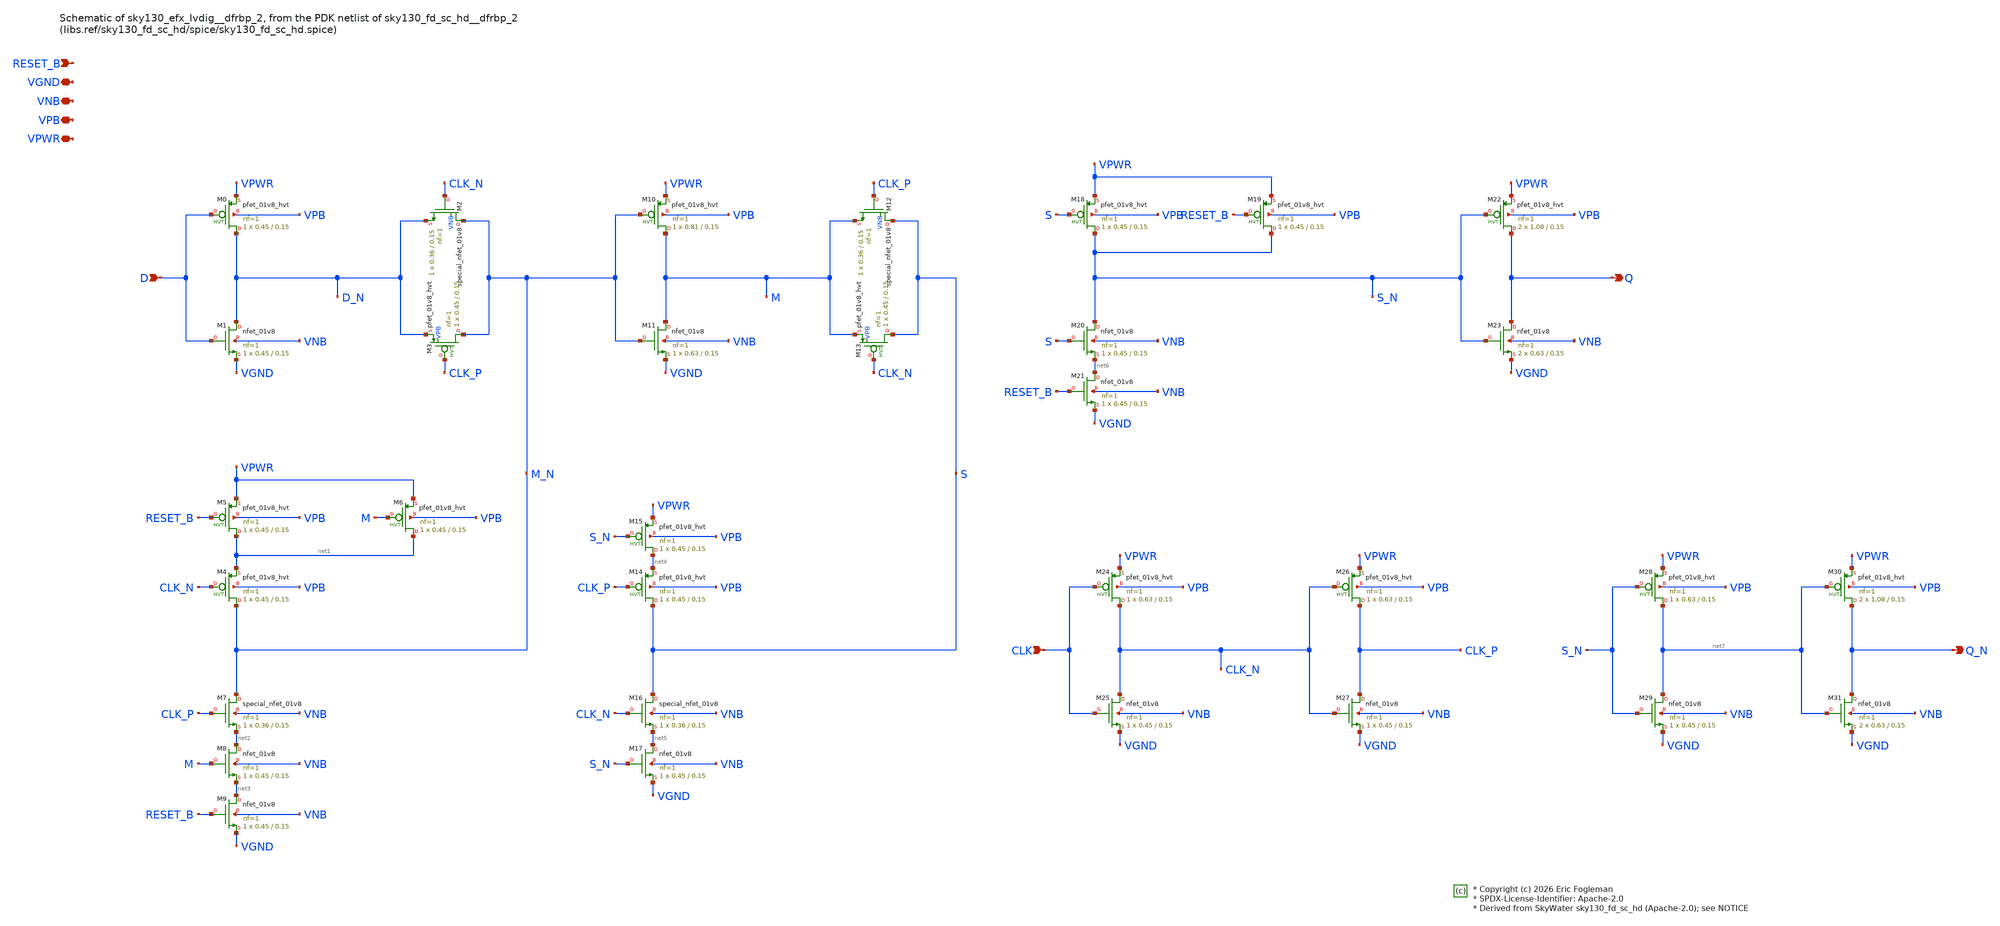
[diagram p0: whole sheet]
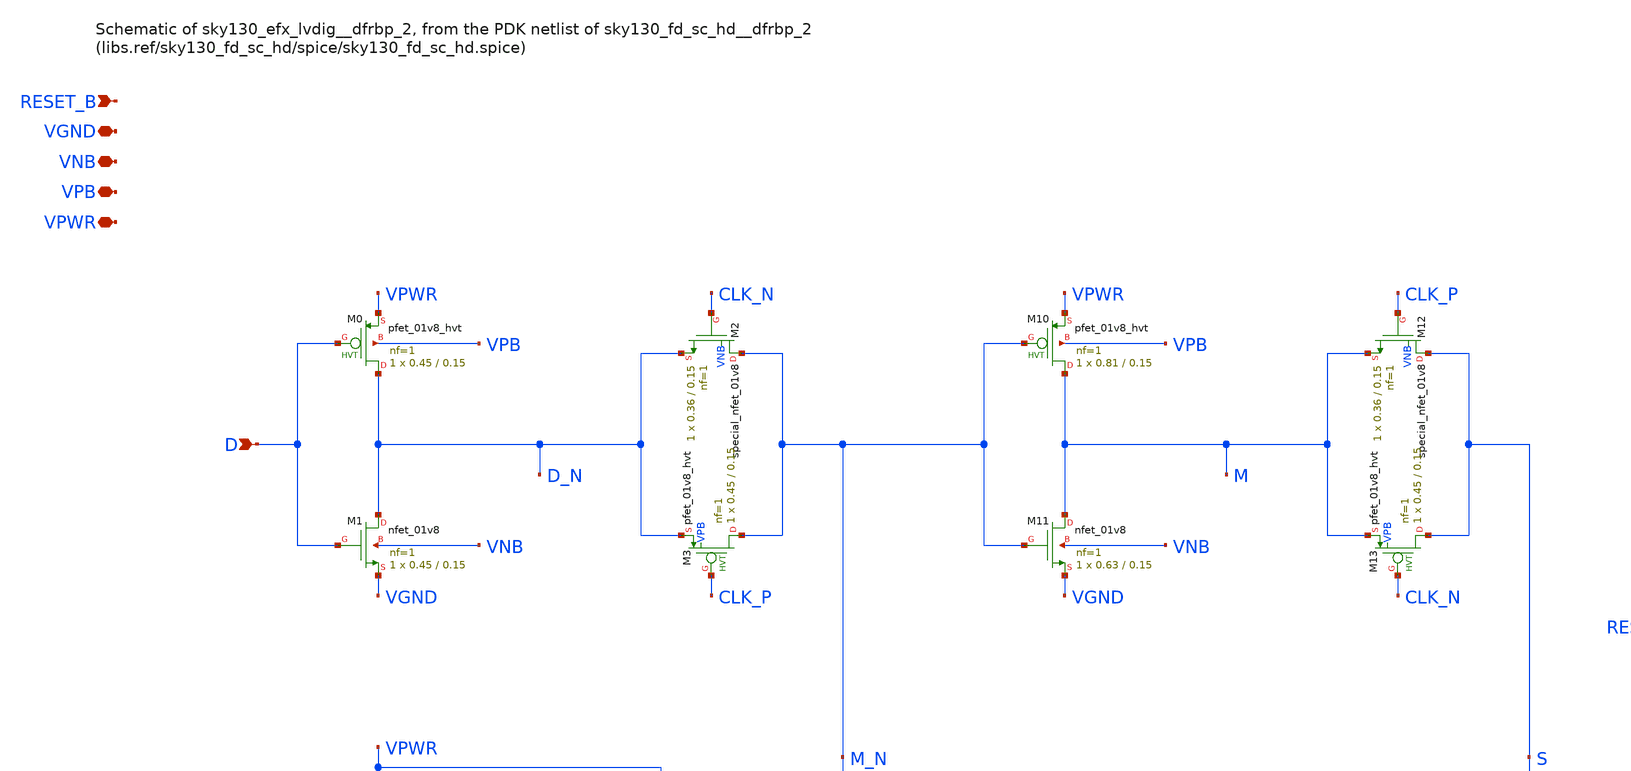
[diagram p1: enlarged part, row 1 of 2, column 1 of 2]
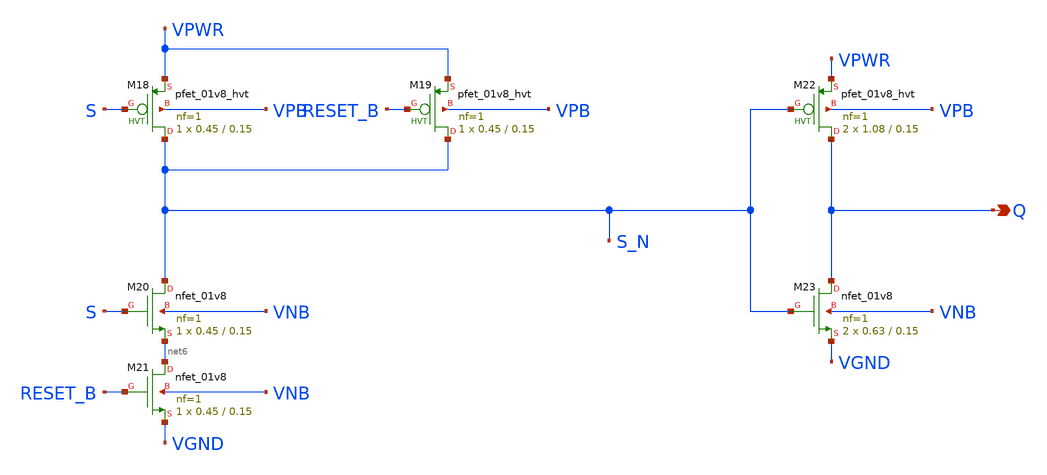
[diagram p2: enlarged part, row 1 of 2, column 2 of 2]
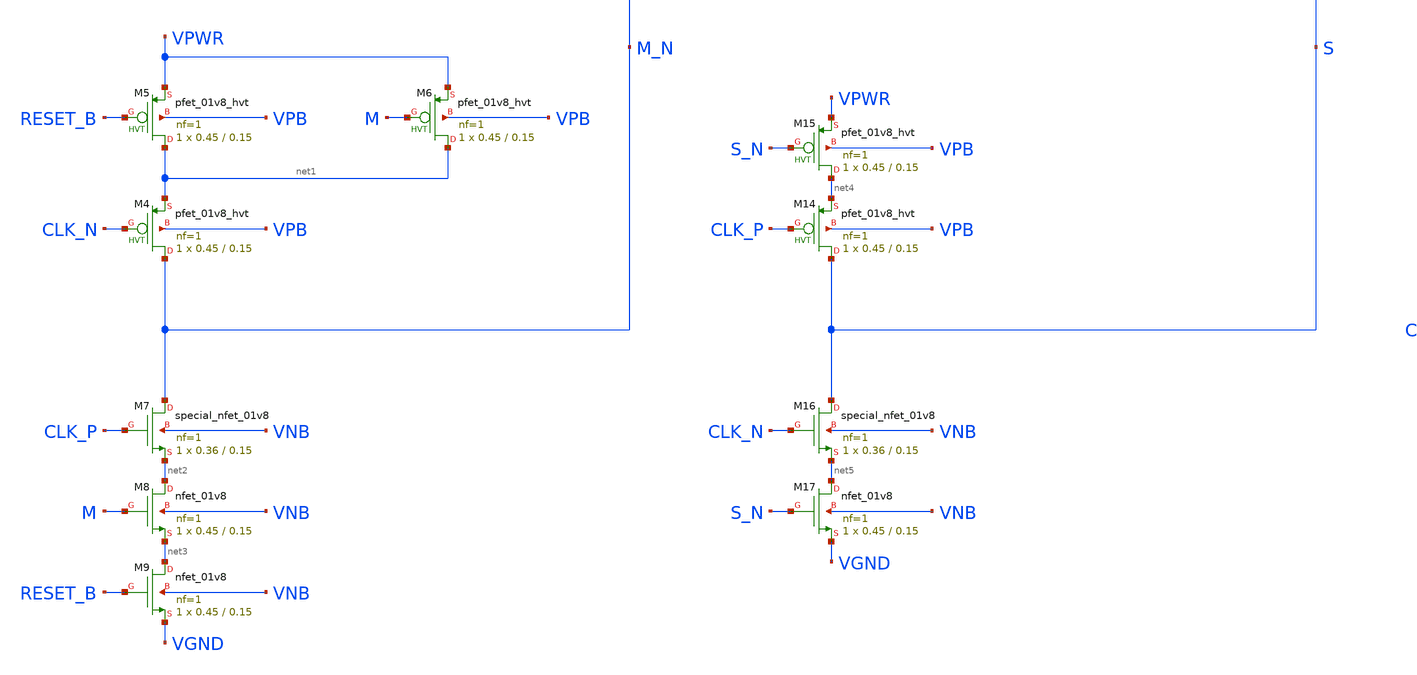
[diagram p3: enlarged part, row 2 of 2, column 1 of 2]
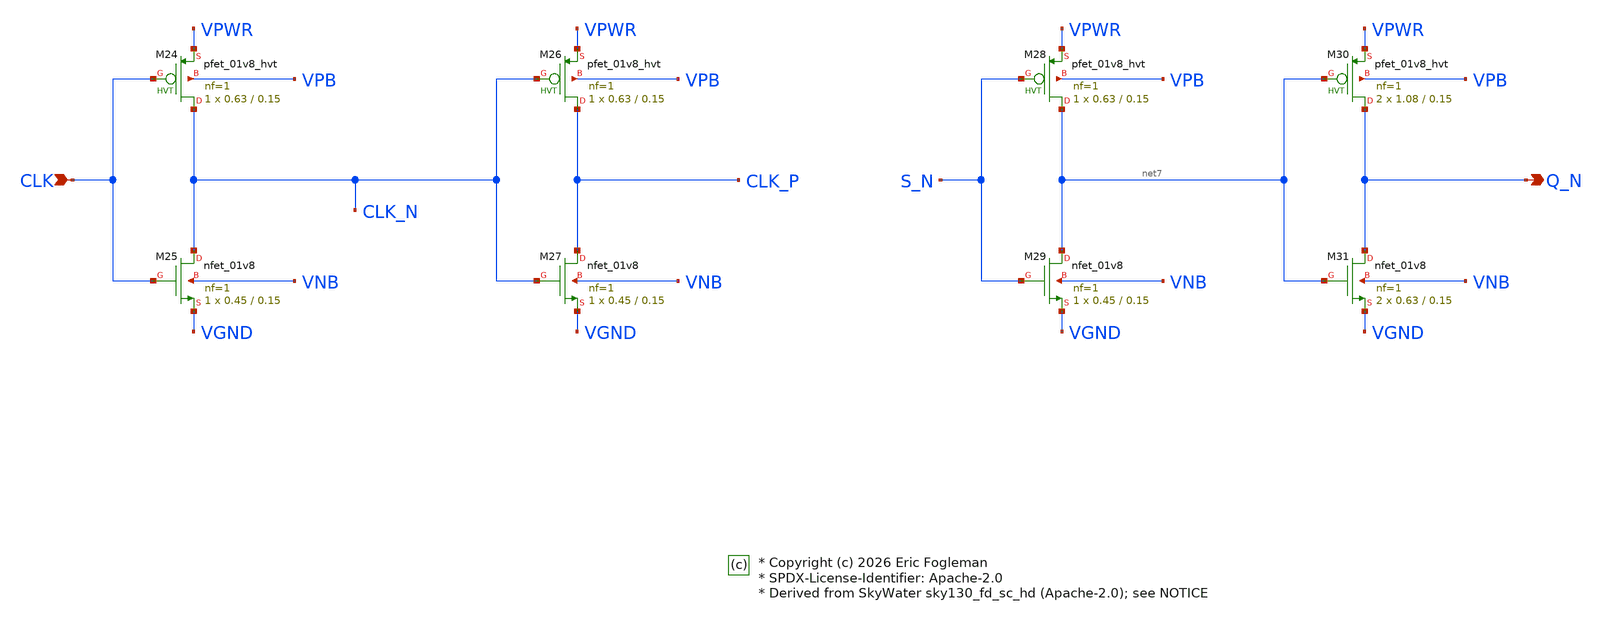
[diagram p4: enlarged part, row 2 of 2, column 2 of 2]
** sch_path: xschem/sky130_efx_lvdig__dfrbp_2.sch

* Copyright (c) 2026 Eric Fogleman
* SPDX-License-Identifier: Apache-2.0
* Derived from SkyWater sky130_fd_sc_hd (Apache-2.0); see NOTICE

**.subckt sky130_efx_lvdig__dfrbp_2 D Q CLK Q_N RESET_B VGND VNB VPB VPWR
*.ipin D
*.opin Q
*.ipin CLK
*.opin Q_N
*.ipin RESET_B
*.iopin VGND
*.iopin VNB
*.iopin VPB
*.iopin VPWR
XM0 D_N D VPWR VPB sky130_fd_pr__pfet_01v8_hvt L=0.15 W=0.45 nf=1 ad='int((1 + 1)/2) * 0.45 / 1 * 0.29'
+ as='int((1 + 2)/2) * 0.45 / 1 * 0.29' pd='2*int((1 + 1)/2) * (0.45 / 1 + 0.29)' ps='2*int((1 + 2)/2) * (0.45 / 1 + 0.29)'
+ nrd='0.29 / 0.45 ' nrs='0.29 / 0.45 ' sa=0 sb=0 sd=0 mult=1 m=1
XM1 D_N D VGND VNB sky130_fd_pr__nfet_01v8 L=0.15 W=0.45 nf=1 ad='int((1 + 1)/2) * 0.45 / 1 * 0.29' as='int((1 + 2)/2) * 0.45 / 1 * 0.29'
+ pd='2*int((1 + 1)/2) * (0.45 / 1 + 0.29)' ps='2*int((1 + 2)/2) * (0.45 / 1 + 0.29)' nrd='0.29 / 0.45 '
+ nrs='0.29 / 0.45 ' sa=0 sb=0 sd=0 mult=1 m=1
XM2 M_N CLK_N D_N VNB sky130_fd_pr__special_nfet_01v8 L=0.15 W=0.36 nf=1 ad='int((nf+1)/2) * W/nf * 0.29'
+ as='int((nf+2)/2) * W/nf * 0.29' pd='2*int((nf+1)/2) * (W/nf + 0.29)' ps='2*int((nf+2)/2) * (W/nf + 0.29)'
+ nrd='0.29 / W' nrs='0.29 / W' sa=0 sb=0 sd=0 mult=1 m=1
XM3 M_N CLK_P D_N VPB sky130_fd_pr__pfet_01v8_hvt L=0.15 W=0.45 nf=1 ad='int((1 + 1)/2) * 0.45 / 1 * 0.29'
+ as='int((1 + 2)/2) * 0.45 / 1 * 0.29' pd='2*int((1 + 1)/2) * (0.45 / 1 + 0.29)' ps='2*int((1 + 2)/2) * (0.45 / 1 + 0.29)'
+ nrd='0.29 / 0.45 ' nrs='0.29 / 0.45 ' sa=0 sb=0 sd=0 mult=1 m=1
XM4 M_N CLK_N net1 VPB sky130_fd_pr__pfet_01v8_hvt L=0.15 W=0.45 nf=1 ad='int((1 + 1)/2) * 0.45 / 1 * 0.29'
+ as='int((1 + 2)/2) * 0.45 / 1 * 0.29' pd='2*int((1 + 1)/2) * (0.45 / 1 + 0.29)' ps='2*int((1 + 2)/2) * (0.45 / 1 + 0.29)'
+ nrd='0.29 / 0.45 ' nrs='0.29 / 0.45 ' sa=0 sb=0 sd=0 mult=1 m=1
XM5 net1 RESET_B VPWR VPB sky130_fd_pr__pfet_01v8_hvt L=0.15 W=0.45 nf=1 ad='int((1 + 1)/2) * 0.45 / 1 * 0.29'
+ as='int((1 + 2)/2) * 0.45 / 1 * 0.29' pd='2*int((1 + 1)/2) * (0.45 / 1 + 0.29)' ps='2*int((1 + 2)/2) * (0.45 / 1 + 0.29)'
+ nrd='0.29 / 0.45 ' nrs='0.29 / 0.45 ' sa=0 sb=0 sd=0 mult=1 m=1
XM6 net1 M VPWR VPB sky130_fd_pr__pfet_01v8_hvt L=0.15 W=0.45 nf=1 ad='int((1 + 1)/2) * 0.45 / 1 * 0.29'
+ as='int((1 + 2)/2) * 0.45 / 1 * 0.29' pd='2*int((1 + 1)/2) * (0.45 / 1 + 0.29)' ps='2*int((1 + 2)/2) * (0.45 / 1 + 0.29)'
+ nrd='0.29 / 0.45 ' nrs='0.29 / 0.45 ' sa=0 sb=0 sd=0 mult=1 m=1
XM7 M_N CLK_P net2 VNB sky130_fd_pr__special_nfet_01v8 L=0.15 W=0.36 nf=1 ad='int((1 + 1)/2) * 0.36 / 1 * 0.29'
+ as='int((1 + 2)/2) * 0.36 / 1 * 0.29' pd='2*int((1 + 1)/2) * (0.36 / 1 + 0.29)' ps='2*int((1 + 2)/2) * (0.36 / 1 + 0.29)'
+ nrd='0.29 / 0.36 ' nrs='0.29 / 0.36 ' sa=0 sb=0 sd=0 mult=1 m=1
XM8 net2 M net3 VNB sky130_fd_pr__nfet_01v8 L=0.15 W=0.45 nf=1 ad='int((1 + 1)/2) * 0.45 / 1 * 0.29'
+ as='int((1 + 2)/2) * 0.45 / 1 * 0.29' pd='2*int((1 + 1)/2) * (0.45 / 1 + 0.29)' ps='2*int((1 + 2)/2) * (0.45 / 1 + 0.29)'
+ nrd='0.29 / 0.45 ' nrs='0.29 / 0.45 ' sa=0 sb=0 sd=0 mult=1 m=1
XM9 net3 RESET_B VGND VNB sky130_fd_pr__nfet_01v8 L=0.15 W=0.45 nf=1 ad='int((1 + 1)/2) * 0.45 / 1 * 0.29'
+ as='int((1 + 2)/2) * 0.45 / 1 * 0.29' pd='2*int((1 + 1)/2) * (0.45 / 1 + 0.29)' ps='2*int((1 + 2)/2) * (0.45 / 1 + 0.29)'
+ nrd='0.29 / 0.45 ' nrs='0.29 / 0.45 ' sa=0 sb=0 sd=0 mult=1 m=1
XM10 M M_N VPWR VPB sky130_fd_pr__pfet_01v8_hvt L=0.15 W=0.81 nf=1 ad='int((1 + 1)/2) * 0.81 / 1 * 0.29'
+ as='int((1 + 2)/2) * 0.81 / 1 * 0.29' pd='2*int((1 + 1)/2) * (0.81 / 1 + 0.29)' ps='2*int((1 + 2)/2) * (0.81 / 1 + 0.29)'
+ nrd='0.29 / 0.81 ' nrs='0.29 / 0.81 ' sa=0 sb=0 sd=0 mult=1 m=1
XM11 M M_N VGND VNB sky130_fd_pr__nfet_01v8 L=0.15 W=0.63 nf=1 ad='int((1 + 1)/2) * 0.63 / 1 * 0.29'
+ as='int((1 + 2)/2) * 0.63 / 1 * 0.29' pd='2*int((1 + 1)/2) * (0.63 / 1 + 0.29)' ps='2*int((1 + 2)/2) * (0.63 / 1 + 0.29)'
+ nrd='0.29 / 0.63 ' nrs='0.29 / 0.63 ' sa=0 sb=0 sd=0 mult=1 m=1
XM12 S CLK_P M VNB sky130_fd_pr__special_nfet_01v8 L=0.15 W=0.36 nf=1 ad='int((nf+1)/2) * W/nf * 0.29'
+ as='int((nf+2)/2) * W/nf * 0.29' pd='2*int((nf+1)/2) * (W/nf + 0.29)' ps='2*int((nf+2)/2) * (W/nf + 0.29)'
+ nrd='0.29 / W' nrs='0.29 / W' sa=0 sb=0 sd=0 mult=1 m=1
XM13 S CLK_N M VPB sky130_fd_pr__pfet_01v8_hvt L=0.15 W=0.45 nf=1 ad='int((1 + 1)/2) * 0.45 / 1 * 0.29'
+ as='int((1 + 2)/2) * 0.45 / 1 * 0.29' pd='2*int((1 + 1)/2) * (0.45 / 1 + 0.29)' ps='2*int((1 + 2)/2) * (0.45 / 1 + 0.29)'
+ nrd='0.29 / 0.45 ' nrs='0.29 / 0.45 ' sa=0 sb=0 sd=0 mult=1 m=1
XM14 S CLK_P net4 VPB sky130_fd_pr__pfet_01v8_hvt L=0.15 W=0.45 nf=1 ad='int((1 + 1)/2) * 0.45 / 1 * 0.29'
+ as='int((1 + 2)/2) * 0.45 / 1 * 0.29' pd='2*int((1 + 1)/2) * (0.45 / 1 + 0.29)' ps='2*int((1 + 2)/2) * (0.45 / 1 + 0.29)'
+ nrd='0.29 / 0.45 ' nrs='0.29 / 0.45 ' sa=0 sb=0 sd=0 mult=1 m=1
XM15 net4 S_N VPWR VPB sky130_fd_pr__pfet_01v8_hvt L=0.15 W=0.45 nf=1 ad='int((1 + 1)/2) * 0.45 / 1 * 0.29'
+ as='int((1 + 2)/2) * 0.45 / 1 * 0.29' pd='2*int((1 + 1)/2) * (0.45 / 1 + 0.29)' ps='2*int((1 + 2)/2) * (0.45 / 1 + 0.29)'
+ nrd='0.29 / 0.45 ' nrs='0.29 / 0.45 ' sa=0 sb=0 sd=0 mult=1 m=1
XM16 S CLK_N net5 VNB sky130_fd_pr__special_nfet_01v8 L=0.15 W=0.36 nf=1 ad='int((1 + 1)/2) * 0.36 / 1 * 0.29'
+ as='int((1 + 2)/2) * 0.36 / 1 * 0.29' pd='2*int((1 + 1)/2) * (0.36 / 1 + 0.29)' ps='2*int((1 + 2)/2) * (0.36 / 1 + 0.29)'
+ nrd='0.29 / 0.36 ' nrs='0.29 / 0.36 ' sa=0 sb=0 sd=0 mult=1 m=1
XM17 net5 S_N VGND VNB sky130_fd_pr__nfet_01v8 L=0.15 W=0.45 nf=1 ad='int((1 + 1)/2) * 0.45 / 1 * 0.29'
+ as='int((1 + 2)/2) * 0.45 / 1 * 0.29' pd='2*int((1 + 1)/2) * (0.45 / 1 + 0.29)' ps='2*int((1 + 2)/2) * (0.45 / 1 + 0.29)'
+ nrd='0.29 / 0.45 ' nrs='0.29 / 0.45 ' sa=0 sb=0 sd=0 mult=1 m=1
XM18 S_N S VPWR VPB sky130_fd_pr__pfet_01v8_hvt L=0.15 W=0.45 nf=1 ad='int((1 + 1)/2) * 0.45 / 1 * 0.29'
+ as='int((1 + 2)/2) * 0.45 / 1 * 0.29' pd='2*int((1 + 1)/2) * (0.45 / 1 + 0.29)' ps='2*int((1 + 2)/2) * (0.45 / 1 + 0.29)'
+ nrd='0.29 / 0.45 ' nrs='0.29 / 0.45 ' sa=0 sb=0 sd=0 mult=1 m=1
XM19 S_N RESET_B VPWR VPB sky130_fd_pr__pfet_01v8_hvt L=0.15 W=0.45 nf=1 ad='int((1 + 1)/2) * 0.45 / 1 * 0.29'
+ as='int((1 + 2)/2) * 0.45 / 1 * 0.29' pd='2*int((1 + 1)/2) * (0.45 / 1 + 0.29)' ps='2*int((1 + 2)/2) * (0.45 / 1 + 0.29)'
+ nrd='0.29 / 0.45 ' nrs='0.29 / 0.45 ' sa=0 sb=0 sd=0 mult=1 m=1
XM20 S_N S net6 VNB sky130_fd_pr__nfet_01v8 L=0.15 W=0.45 nf=1 ad='int((1 + 1)/2) * 0.45 / 1 * 0.29'
+ as='int((1 + 2)/2) * 0.45 / 1 * 0.29' pd='2*int((1 + 1)/2) * (0.45 / 1 + 0.29)' ps='2*int((1 + 2)/2) * (0.45 / 1 + 0.29)'
+ nrd='0.29 / 0.45 ' nrs='0.29 / 0.45 ' sa=0 sb=0 sd=0 mult=1 m=1
XM21 net6 RESET_B VGND VNB sky130_fd_pr__nfet_01v8 L=0.15 W=0.45 nf=1 ad='int((1 + 1)/2) * 0.45 / 1 * 0.29'
+ as='int((1 + 2)/2) * 0.45 / 1 * 0.29' pd='2*int((1 + 1)/2) * (0.45 / 1 + 0.29)' ps='2*int((1 + 2)/2) * (0.45 / 1 + 0.29)'
+ nrd='0.29 / 0.45 ' nrs='0.29 / 0.45 ' sa=0 sb=0 sd=0 mult=1 m=1
XM22 Q S_N VPWR VPB sky130_fd_pr__pfet_01v8_hvt L=0.15 W=1.08 nf=1 ad='int((1 + 1)/2) * 1.08 / 1 * 0.29'
+ as='int((1 + 2)/2) * 1.08 / 1 * 0.29' pd='2*int((1 + 1)/2) * (1.08 / 1 + 0.29)' ps='2*int((1 + 2)/2) * (1.08 / 1 + 0.29)'
+ nrd='0.29 / 1.08 ' nrs='0.29 / 1.08 ' sa=0 sb=0 sd=0 mult=2 m=2
XM23 Q S_N VGND VNB sky130_fd_pr__nfet_01v8 L=0.15 W=0.63 nf=1 ad='int((1 + 1)/2) * 0.63 / 1 * 0.29'
+ as='int((1 + 2)/2) * 0.63 / 1 * 0.29' pd='2*int((1 + 1)/2) * (0.63 / 1 + 0.29)' ps='2*int((1 + 2)/2) * (0.63 / 1 + 0.29)'
+ nrd='0.29 / 0.63 ' nrs='0.29 / 0.63 ' sa=0 sb=0 sd=0 mult=2 m=2
XM24 CLK_N CLK VPWR VPB sky130_fd_pr__pfet_01v8_hvt L=0.15 W=0.63 nf=1 ad='int((1 + 1)/2) * 0.63 / 1 * 0.29'
+ as='int((1 + 2)/2) * 0.63 / 1 * 0.29' pd='2*int((1 + 1)/2) * (0.63 / 1 + 0.29)' ps='2*int((1 + 2)/2) * (0.63 / 1 + 0.29)'
+ nrd='0.29 / 0.63 ' nrs='0.29 / 0.63 ' sa=0 sb=0 sd=0 mult=1 m=1
XM25 CLK_N CLK VGND VNB sky130_fd_pr__nfet_01v8 L=0.15 W=0.45 nf=1 ad='int((1 + 1)/2) * 0.45 / 1 * 0.29'
+ as='int((1 + 2)/2) * 0.45 / 1 * 0.29' pd='2*int((1 + 1)/2) * (0.45 / 1 + 0.29)' ps='2*int((1 + 2)/2) * (0.45 / 1 + 0.29)'
+ nrd='0.29 / 0.45 ' nrs='0.29 / 0.45 ' sa=0 sb=0 sd=0 mult=1 m=1
XM26 CLK_P CLK_N VPWR VPB sky130_fd_pr__pfet_01v8_hvt L=0.15 W=0.63 nf=1 ad='int((1 + 1)/2) * 0.63 / 1 * 0.29'
+ as='int((1 + 2)/2) * 0.63 / 1 * 0.29' pd='2*int((1 + 1)/2) * (0.63 / 1 + 0.29)' ps='2*int((1 + 2)/2) * (0.63 / 1 + 0.29)'
+ nrd='0.29 / 0.63 ' nrs='0.29 / 0.63 ' sa=0 sb=0 sd=0 mult=1 m=1
XM27 CLK_P CLK_N VGND VNB sky130_fd_pr__nfet_01v8 L=0.15 W=0.45 nf=1 ad='int((1 + 1)/2) * 0.45 / 1 * 0.29'
+ as='int((1 + 2)/2) * 0.45 / 1 * 0.29' pd='2*int((1 + 1)/2) * (0.45 / 1 + 0.29)' ps='2*int((1 + 2)/2) * (0.45 / 1 + 0.29)'
+ nrd='0.29 / 0.45 ' nrs='0.29 / 0.45 ' sa=0 sb=0 sd=0 mult=1 m=1
XM28 net7 S_N VPWR VPB sky130_fd_pr__pfet_01v8_hvt L=0.15 W=0.63 nf=1 ad='int((1 + 1)/2) * 0.63 / 1 * 0.29'
+ as='int((1 + 2)/2) * 0.63 / 1 * 0.29' pd='2*int((1 + 1)/2) * (0.63 / 1 + 0.29)' ps='2*int((1 + 2)/2) * (0.63 / 1 + 0.29)'
+ nrd='0.29 / 0.63 ' nrs='0.29 / 0.63 ' sa=0 sb=0 sd=0 mult=1 m=1
XM29 net7 S_N VGND VNB sky130_fd_pr__nfet_01v8 L=0.15 W=0.45 nf=1 ad='int((1 + 1)/2) * 0.45 / 1 * 0.29'
+ as='int((1 + 2)/2) * 0.45 / 1 * 0.29' pd='2*int((1 + 1)/2) * (0.45 / 1 + 0.29)' ps='2*int((1 + 2)/2) * (0.45 / 1 + 0.29)'
+ nrd='0.29 / 0.45 ' nrs='0.29 / 0.45 ' sa=0 sb=0 sd=0 mult=1 m=1
XM30 Q_N net7 VPWR VPB sky130_fd_pr__pfet_01v8_hvt L=0.15 W=1.08 nf=1 ad='int((1 + 1)/2) * 1.08 / 1 * 0.29'
+ as='int((1 + 2)/2) * 1.08 / 1 * 0.29' pd='2*int((1 + 1)/2) * (1.08 / 1 + 0.29)' ps='2*int((1 + 2)/2) * (1.08 / 1 + 0.29)'
+ nrd='0.29 / 1.08 ' nrs='0.29 / 1.08 ' sa=0 sb=0 sd=0 mult=2 m=2
XM31 Q_N net7 VGND VNB sky130_fd_pr__nfet_01v8 L=0.15 W=0.63 nf=1 ad='int((1 + 1)/2) * 0.63 / 1 * 0.29'
+ as='int((1 + 2)/2) * 0.63 / 1 * 0.29' pd='2*int((1 + 1)/2) * (0.63 / 1 + 0.29)' ps='2*int((1 + 2)/2) * (0.63 / 1 + 0.29)'
+ nrd='0.29 / 0.63 ' nrs='0.29 / 0.63 ' sa=0 sb=0 sd=0 mult=2 m=2
**.ends
.end
